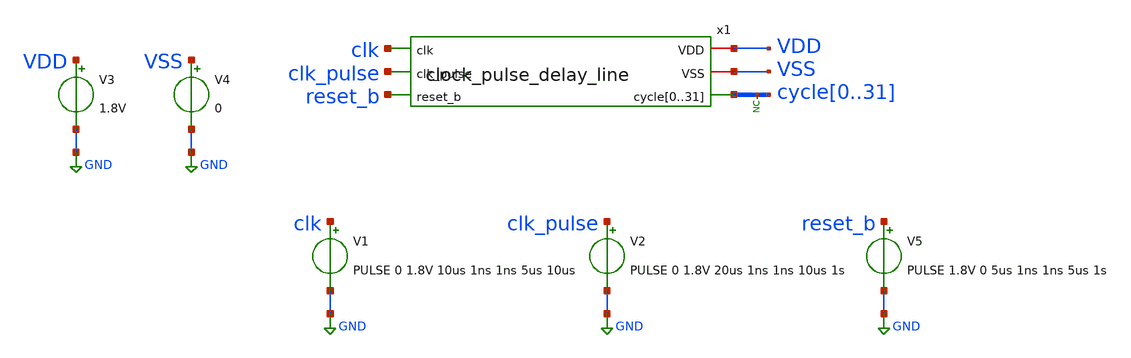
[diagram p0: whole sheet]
** sch_path: xschem/tests/clock_pulse_delay_line/clock_pulse_delay_line_test.sch
**.subckt clock_pulse_delay_line_test
V3 VDD GND 1.8V
V4 VSS GND 0
x1 clk VDD VSS clk_pulse reset_b cycle0 cycle1 cycle2 cycle3 cycle4 cycle5 cycle6 cycle7 cycle8
+ cycle9 cycle10 cycle11 cycle12 cycle13 cycle14 cycle15 cycle16 cycle17 cycle18 cycle19 cycle20 cycle21
+ cycle22 cycle23 cycle24 cycle25 cycle26 cycle27 cycle28 cycle29 cycle30 cycle31 clock_pulse_delay_line
* noconn cycle[0..31]
V1 clk GND PULSE 0 1.8V 10us 1ns 1ns 5us 10us
V2 clk_pulse GND PULSE 0 1.8V 20us 1ns 1ns 10us 1s
V5 reset_b GND PULSE 1.8V 0 5us 1ns 1ns 5us 1s
**** begin user architecture code
 .lib $::SKYWATER_MODELS/sky130.lib.spice tt
.include $::SKYWATER_STDCELLS/sky130_fd_sc_hd.spice


.options acct list
.temp 25
*vvcc VDD 0 dc 1.8
*vvss VSS 0 0
.control
tran 0.1u 350u
*plot RST_PLS clk+2 Pulse+4
plot reset_b-6 clk-4 clk_pulse-2 cycle0 cycle1+2 cycle2+4 cycle3+6 cycle4+8 cycle5+10 cycle6+12
+ cycle7+14 cycle8+16 cycle9+18 cycle10+20 cycle11+22 cycle12+24 cycle13+26 cycle14+28 cycle15+30 cycle16+32
+ cycle17+34 cycle18+36 cycle19+38 cycle20+40 cycle21+42 cycle22+44  cycle23+46 cycle24+48 cycle25+50 cycle26+52
+ cycle27+54 cycle28+56 cycle29+58 cycle30+60 cycle31+62

write clock_pulse_delay_line.raw
.endc


**** end user architecture code
**.ends

* expanding   symbol:  src/clock_pulse_delay_line/clock_pulse_delay_line.sym # of pins=6
** sym_path: xschem/src/clock_pulse_delay_line/clock_pulse_delay_line.sym
** sch_path: xschem/src/clock_pulse_delay_line/clock_pulse_delay_line.sch
.subckt clock_pulse_delay_line clk VDD VSS clk_pulse reset_b cycle0 cycle1 cycle2 cycle3 cycle4
+ cycle5 cycle6 cycle7 cycle8 cycle9 cycle10 cycle11 cycle12 cycle13 cycle14 cycle15 cycle16 cycle17 cycle18
+ cycle19 cycle20 cycle21 cycle22 cycle23 cycle24 cycle25 cycle26 cycle27 cycle28 cycle29 cycle30 cycle31
*.ipin clk_pulse
*.opin
*+ cycle0,cycle1,cycle2,cycle3,cycle4,cycle5,cycle6,cycle7,cycle8,cycle9,cycle10,cycle11,cycle12,cycle13,cycle14,cycle15,cycle16,cycle17,cycle18,cycle19,cycle20,cycle21,cycle22,cycle23,cycle24,cycle25,cycle26,cycle27,cycle28,cycle29,cycle30,cycle31
*.iopin VSS
*.iopin VDD
*.ipin clk
*.ipin reset_b
* noconn cycle31
x3 clk clk_pulse reset_b VSS VSS VDD VDD cycle1 sky130_fd_sc_hd__dfrtn_1
x1 clk cycle1 reset_b VSS VSS VDD VDD cycle2 sky130_fd_sc_hd__dfrtn_1
x24 clk cycle2 reset_b VSS VSS VDD VDD cycle3 sky130_fd_sc_hd__dfrtn_1
x26 clk cycle3 reset_b VSS VSS VDD VDD cycle4 sky130_fd_sc_hd__dfrtn_1
x28 clk cycle4 reset_b VSS VSS VDD VDD cycle5 sky130_fd_sc_hd__dfrtn_1
x21 clk cycle5 reset_b VSS VSS VDD VDD cycle6 sky130_fd_sc_hd__dfrtn_1
x23 clk cycle6 reset_b VSS VSS VDD VDD cycle7 sky130_fd_sc_hd__dfrtn_1
x25 clk cycle7 reset_b VSS VSS VDD VDD cycle8 sky130_fd_sc_hd__dfrtn_1
x27 clk cycle8 reset_b VSS VSS VDD VDD cycle9 sky130_fd_sc_hd__dfrtn_1
x29 clk cycle9 reset_b VSS VSS VDD VDD cycle10 sky130_fd_sc_hd__dfrtn_1
x30 clk cycle10 reset_b VSS VSS VDD VDD cycle11 sky130_fd_sc_hd__dfrtn_1
x31 clk cycle11 reset_b VSS VSS VDD VDD cycle12 sky130_fd_sc_hd__dfrtn_1
x32 clk cycle12 reset_b VSS VSS VDD VDD cycle13 sky130_fd_sc_hd__dfrtn_1
x4 clk cycle13 reset_b VSS VSS VDD VDD cycle14 sky130_fd_sc_hd__dfrtn_1
x5 clk cycle15 reset_b VSS VSS VDD VDD cycle16 sky130_fd_sc_hd__dfrtn_1
x6 clk cycle16 reset_b VSS VSS VDD VDD cycle17 sky130_fd_sc_hd__dfrtn_1
x7 clk cycle17 reset_b VSS VSS VDD VDD cycle18 sky130_fd_sc_hd__dfrtn_1
x8 clk cycle18 reset_b VSS VSS VDD VDD cycle19 sky130_fd_sc_hd__dfrtn_1
x9 clk cycle19 reset_b VSS VSS VDD VDD cycle20 sky130_fd_sc_hd__dfrtn_1
x10 clk cycle20 reset_b VSS VSS VDD VDD cycle21 sky130_fd_sc_hd__dfrtn_1
x11 clk cycle21 reset_b VSS VSS VDD VDD cycle22 sky130_fd_sc_hd__dfrtn_1
x12 clk cycle22 reset_b VSS VSS VDD VDD cycle23 sky130_fd_sc_hd__dfrtn_1
x13 clk cycle23 reset_b VSS VSS VDD VDD cycle24 sky130_fd_sc_hd__dfrtn_1
x14 clk cycle24 reset_b VSS VSS VDD VDD cycle25 sky130_fd_sc_hd__dfrtn_1
x15 clk cycle25 reset_b VSS VSS VDD VDD cycle26 sky130_fd_sc_hd__dfrtn_1
x16 clk cycle26 reset_b VSS VSS VDD VDD cycle27 sky130_fd_sc_hd__dfrtn_1
x17 clk cycle27 reset_b VSS VSS VDD VDD cycle28 sky130_fd_sc_hd__dfrtn_1
x18 clk cycle28 reset_b VSS VSS VDD VDD cycle29 sky130_fd_sc_hd__dfrtn_1
x19 clk cycle29 reset_b VSS VSS VDD VDD cycle30 sky130_fd_sc_hd__dfrtn_1
x20 clk cycle30 reset_b VSS VSS VDD VDD cycle31 sky130_fd_sc_hd__dfrtn_1
x2 clk cycle14 reset_b VSS VSS VDD VDD cycle15 sky130_fd_sc_hd__dfrtn_1
x33 clk_pulse VSS VSS VDD VDD cycle0 sky130_fd_sc_hd__buf_12
.ends

.GLOBAL GND
.end
